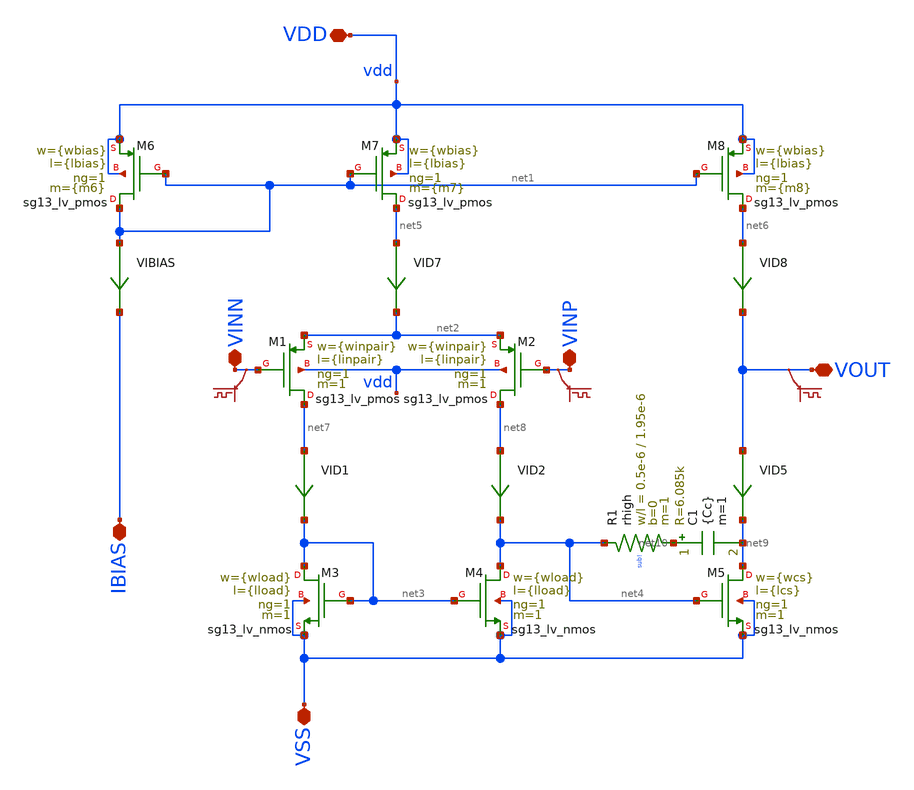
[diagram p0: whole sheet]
** sch_path: designs/libs/core_analog/fine_gain/fine_gain_ota.sch
**.subckt fine_gain_ota IBIAS VDD VSS VOUT VINP VINN
*.iopin IBIAS
*.iopin VDD
*.iopin VSS
*.iopin VOUT
*.iopin VINP
*.iopin VINN
XM6 net1 net1 vdd vdd sg13_lv_pmos w={wbias} l={lbias} ng=1 m={m6} mm_ok=1
XM7 net5 net1 vdd vdd sg13_lv_pmos w={wbias} l={lbias} ng=1 m={m7} mm_ok=1
XM8 net6 net1 vdd vdd sg13_lv_pmos w={wbias} l={lbias} ng=1 m={m8} mm_ok=1
XM1 net7 VINN net2 vdd sg13_lv_pmos w={winpair} l={linpair} ng=1 m=1 mm_ok=1
XM2 net8 VINP net2 vdd sg13_lv_pmos w={winpair} l={linpair} ng=1 m=1 mm_ok=1
XM3 net3 net3 VSS VSS sg13_lv_nmos w={wload} l={lload} ng=1 m=1 mm_ok=1
XM4 net4 net3 VSS VSS sg13_lv_nmos w={wload} l={lload} ng=1 m=1 mm_ok=1
XM5 net9 net4 VSS VSS sg13_lv_nmos w={wcs} l={lcs} ng=1 m=1 mm_ok=1
C1 net10 net9 {Cc} m=1
XR1 net4 net10 sub! rhigh w=0.5e-6 l=1.95e-6 m=1 b=0 mm_ok=1
VIBIAS net1 IBIAS 0
.save i(vibias)
VID7 net5 net2 0
.save i(vid7)
VID8 net6 VOUT 0
.save i(vid8)
.save v(vinp)
.save v(vinn)
.save v(vout)
VID1 net7 net3 0
.save i(vid1)
VID2 net8 net4 0
.save i(vid2)
VID5 VOUT net9 0
.save i(vid5)
**.ends
.end
